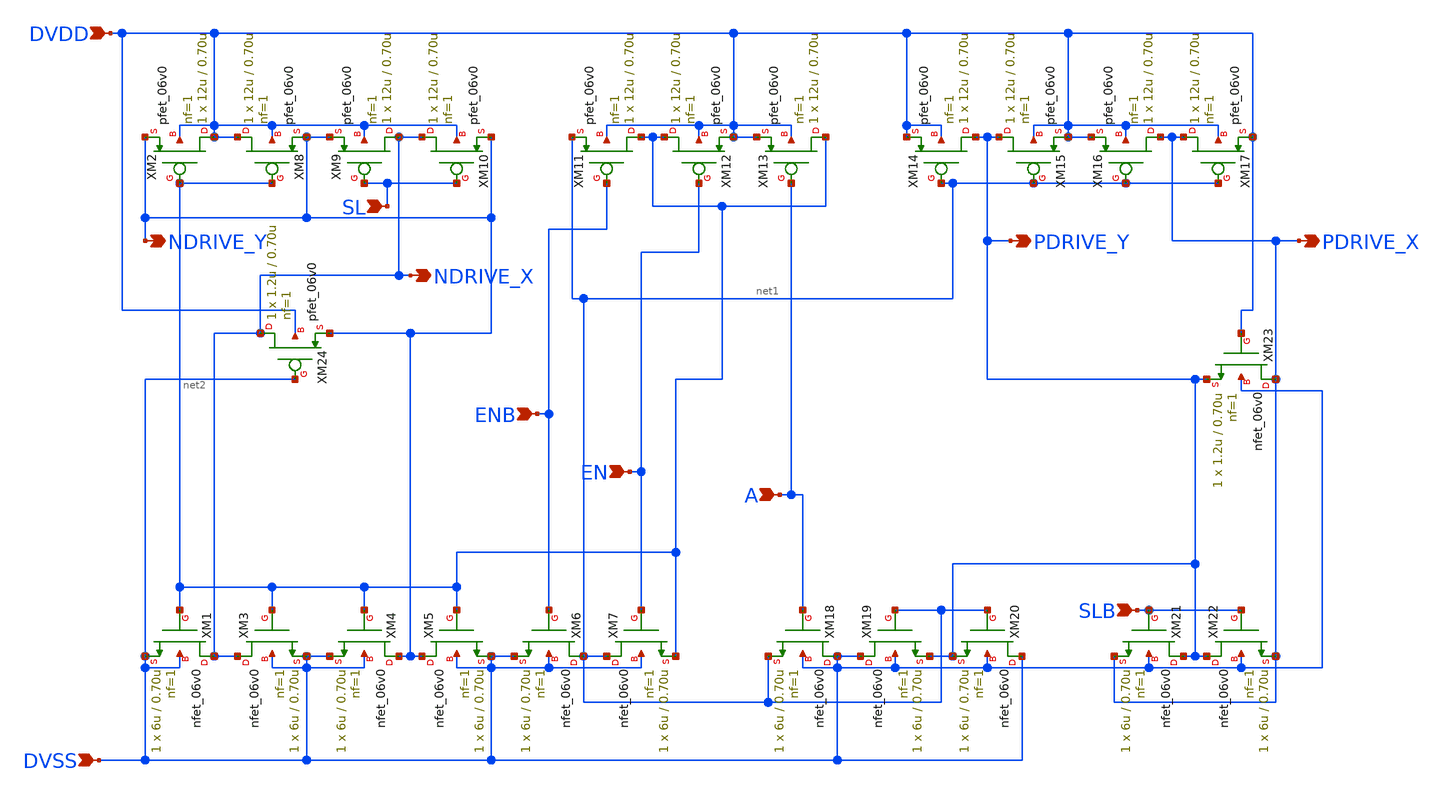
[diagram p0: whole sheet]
** sch_path: gf180mcu_fd_io__bi_24t/comp018green_out_predrv.sch
**.subckt comp018green_out_predrv DVSS DVDD SL ENB EN A SLB NDRIVE_X NDRIVE_Y PDRIVE_X PDRIVE_Y
*.ipin DVSS
*.ipin DVDD
*.ipin SL
*.ipin ENB
*.ipin EN
*.ipin A
*.ipin SLB
*.opin NDRIVE_X
*.opin NDRIVE_Y
*.opin PDRIVE_X
*.opin PDRIVE_Y
XM1 NDRIVE_X net2 DVSS DVSS nfet_06v0 L=0.70u W=6u nf=1 ad='int((nf+1)/2) * W/nf * 0.18u' as='int((nf+2)/2) * W/nf * 0.18u'
+ pd='2*int((nf+1)/2) * (W/nf + 0.18u)' ps='2*int((nf+2)/2) * (W/nf + 0.18u)' nrd='0.18u / W' nrs='0.18u / W'
+ sa=0 sb=0 sd=0 m=1
XM2 DVDD net2 NDRIVE_Y DVDD pfet_06v0 L=0.70u W=12u nf=1 ad='int((nf+1)/2) * W/nf * 0.18u' as='int((nf+2)/2) * W/nf * 0.18u'
+ pd='2*int((nf+1)/2) * (W/nf + 0.18u)' ps='2*int((nf+2)/2) * (W/nf + 0.18u)' nrd='0.18u / W' nrs='0.18u / W'
+ sa=0 sb=0 sd=0 m=1
XM3 NDRIVE_X net2 DVSS DVSS nfet_06v0 L=0.70u W=6u nf=1 ad='int((nf+1)/2) * W/nf * 0.18u' as='int((nf+2)/2) * W/nf * 0.18u'
+ pd='2*int((nf+1)/2) * (W/nf + 0.18u)' ps='2*int((nf+2)/2) * (W/nf + 0.18u)' nrd='0.18u / W' nrs='0.18u / W'
+ sa=0 sb=0 sd=0 m=1
XM4 NDRIVE_Y net2 DVSS DVSS nfet_06v0 L=0.70u W=6u nf=1 ad='int((nf+1)/2) * W/nf * 0.18u' as='int((nf+2)/2) * W/nf * 0.18u'
+ pd='2*int((nf+1)/2) * (W/nf + 0.18u)' ps='2*int((nf+2)/2) * (W/nf + 0.18u)' nrd='0.18u / W' nrs='0.18u / W'
+ sa=0 sb=0 sd=0 m=1
XM5 NDRIVE_Y net2 DVSS DVSS nfet_06v0 L=0.70u W=6u nf=1 ad='int((nf+1)/2) * W/nf * 0.18u' as='int((nf+2)/2) * W/nf * 0.18u'
+ pd='2*int((nf+1)/2) * (W/nf + 0.18u)' ps='2*int((nf+2)/2) * (W/nf + 0.18u)' nrd='0.18u / W' nrs='0.18u / W'
+ sa=0 sb=0 sd=0 m=1
XM6 net1 ENB DVSS DVSS nfet_06v0 L=0.70u W=6u nf=1 ad='int((nf+1)/2) * W/nf * 0.18u' as='int((nf+2)/2) * W/nf * 0.18u'
+ pd='2*int((nf+1)/2) * (W/nf + 0.18u)' ps='2*int((nf+2)/2) * (W/nf + 0.18u)' nrd='0.18u / W' nrs='0.18u / W'
+ sa=0 sb=0 sd=0 m=1
XM7 net1 EN net2 DVSS nfet_06v0 L=0.70u W=6u nf=1 ad='int((nf+1)/2) * W/nf * 0.18u' as='int((nf+2)/2) * W/nf * 0.18u'
+ pd='2*int((nf+1)/2) * (W/nf + 0.18u)' ps='2*int((nf+2)/2) * (W/nf + 0.18u)' nrd='0.18u / W' nrs='0.18u / W'
+ sa=0 sb=0 sd=0 m=1
XM8 DVDD net2 NDRIVE_Y DVDD pfet_06v0 L=0.70u W=12u nf=1 ad='int((nf+1)/2) * W/nf * 0.18u' as='int((nf+2)/2) * W/nf * 0.18u'
+ pd='2*int((nf+1)/2) * (W/nf + 0.18u)' ps='2*int((nf+2)/2) * (W/nf + 0.18u)' nrd='0.18u / W' nrs='0.18u / W'
+ sa=0 sb=0 sd=0 m=1
XM9 NDRIVE_X SL NDRIVE_Y DVDD pfet_06v0 L=0.70u W=12u nf=1 ad='int((nf+1)/2) * W/nf * 0.18u' as='int((nf+2)/2) * W/nf * 0.18u'
+ pd='2*int((nf+1)/2) * (W/nf + 0.18u)' ps='2*int((nf+2)/2) * (W/nf + 0.18u)' nrd='0.18u / W' nrs='0.18u / W'
+ sa=0 sb=0 sd=0 m=1
XM10 NDRIVE_X SL NDRIVE_Y DVDD pfet_06v0 L=0.70u W=12u nf=1 ad='int((nf+1)/2) * W/nf * 0.18u' as='int((nf+2)/2) * W/nf * 0.18u'
+ pd='2*int((nf+1)/2) * (W/nf + 0.18u)' ps='2*int((nf+2)/2) * (W/nf + 0.18u)' nrd='0.18u / W' nrs='0.18u / W'
+ sa=0 sb=0 sd=0 m=1
XM11 net2 ENB net1 DVDD pfet_06v0 L=0.70u W=12u nf=1 ad='int((nf+1)/2) * W/nf * 0.18u' as='int((nf+2)/2) * W/nf * 0.18u'
+ pd='2*int((nf+1)/2) * (W/nf + 0.18u)' ps='2*int((nf+2)/2) * (W/nf + 0.18u)' nrd='0.18u / W' nrs='0.18u / W'
+ sa=0 sb=0 sd=0 m=1
XM12 net2 EN DVDD DVDD pfet_06v0 L=0.70u W=12u nf=1 ad='int((nf+1)/2) * W/nf * 0.18u' as='int((nf+2)/2) * W/nf * 0.18u'
+ pd='2*int((nf+1)/2) * (W/nf + 0.18u)' ps='2*int((nf+2)/2) * (W/nf + 0.18u)' nrd='0.18u / W' nrs='0.18u / W'
+ sa=0 sb=0 sd=0 m=1
XM13 net2 A DVDD DVDD pfet_06v0 L=0.70u W=12u nf=1 ad='int((nf+1)/2) * W/nf * 0.18u' as='int((nf+2)/2) * W/nf * 0.18u'
+ pd='2*int((nf+1)/2) * (W/nf + 0.18u)' ps='2*int((nf+2)/2) * (W/nf + 0.18u)' nrd='0.18u / W' nrs='0.18u / W'
+ sa=0 sb=0 sd=0 m=1
XM14 PDRIVE_Y net1 DVDD DVDD pfet_06v0 L=0.70u W=12u nf=1 ad='int((nf+1)/2) * W/nf * 0.18u' as='int((nf+2)/2) * W/nf * 0.18u'
+ pd='2*int((nf+1)/2) * (W/nf + 0.18u)' ps='2*int((nf+2)/2) * (W/nf + 0.18u)' nrd='0.18u / W' nrs='0.18u / W'
+ sa=0 sb=0 sd=0 m=1
XM15 PDRIVE_Y net1 DVDD DVDD pfet_06v0 L=0.70u W=12u nf=1 ad='int((nf+1)/2) * W/nf * 0.18u' as='int((nf+2)/2) * W/nf * 0.18u'
+ pd='2*int((nf+1)/2) * (W/nf + 0.18u)' ps='2*int((nf+2)/2) * (W/nf + 0.18u)' nrd='0.18u / W' nrs='0.18u / W'
+ sa=0 sb=0 sd=0 m=1
XM16 PDRIVE_X net1 DVDD DVDD pfet_06v0 L=0.70u W=12u nf=1 ad='int((nf+1)/2) * W/nf * 0.18u' as='int((nf+2)/2) * W/nf * 0.18u'
+ pd='2*int((nf+1)/2) * (W/nf + 0.18u)' ps='2*int((nf+2)/2) * (W/nf + 0.18u)' nrd='0.18u / W' nrs='0.18u / W'
+ sa=0 sb=0 sd=0 m=1
XM17 PDRIVE_X net1 DVDD DVDD pfet_06v0 L=0.70u W=12u nf=1 ad='int((nf+1)/2) * W/nf * 0.18u' as='int((nf+2)/2) * W/nf * 0.18u'
+ pd='2*int((nf+1)/2) * (W/nf + 0.18u)' ps='2*int((nf+2)/2) * (W/nf + 0.18u)' nrd='0.18u / W' nrs='0.18u / W'
+ sa=0 sb=0 sd=0 m=1
XM18 DVSS A net1 DVSS nfet_06v0 L=0.70u W=6u nf=1 ad='int((nf+1)/2) * W/nf * 0.18u' as='int((nf+2)/2) * W/nf * 0.18u'
+ pd='2*int((nf+1)/2) * (W/nf + 0.18u)' ps='2*int((nf+2)/2) * (W/nf + 0.18u)' nrd='0.18u / W' nrs='0.18u / W'
+ sa=0 sb=0 sd=0 m=1
XM19 DVSS net1 PDRIVE_Y DVSS nfet_06v0 L=0.70u W=6u nf=1 ad='int((nf+1)/2) * W/nf * 0.18u' as='int((nf+2)/2) * W/nf * 0.18u'
+ pd='2*int((nf+1)/2) * (W/nf + 0.18u)' ps='2*int((nf+2)/2) * (W/nf + 0.18u)' nrd='0.18u / W' nrs='0.18u / W'
+ sa=0 sb=0 sd=0 m=1
XM20 DVSS net1 PDRIVE_Y DVSS nfet_06v0 L=0.70u W=6u nf=1 ad='int((nf+1)/2) * W/nf * 0.18u' as='int((nf+2)/2) * W/nf * 0.18u'
+ pd='2*int((nf+1)/2) * (W/nf + 0.18u)' ps='2*int((nf+2)/2) * (W/nf + 0.18u)' nrd='0.18u / W' nrs='0.18u / W'
+ sa=0 sb=0 sd=0 m=1
XM21 PDRIVE_Y SLB PDRIVE_X DVSS nfet_06v0 L=0.70u W=6u nf=1 ad='int((nf+1)/2) * W/nf * 0.18u' as='int((nf+2)/2) * W/nf * 0.18u'
+ pd='2*int((nf+1)/2) * (W/nf + 0.18u)' ps='2*int((nf+2)/2) * (W/nf + 0.18u)' nrd='0.18u / W' nrs='0.18u / W'
+ sa=0 sb=0 sd=0 m=1
XM22 PDRIVE_Y SLB PDRIVE_X DVSS nfet_06v0 L=0.70u W=6u nf=1 ad='int((nf+1)/2) * W/nf * 0.18u' as='int((nf+2)/2) * W/nf * 0.18u'
+ pd='2*int((nf+1)/2) * (W/nf + 0.18u)' ps='2*int((nf+2)/2) * (W/nf + 0.18u)' nrd='0.18u / W' nrs='0.18u / W'
+ sa=0 sb=0 sd=0 m=1
XM23 PDRIVE_X DVDD PDRIVE_Y DVSS nfet_06v0 L=0.70u W=1.2u nf=1 ad='int((nf+1)/2) * W/nf * 0.18u' as='int((nf+2)/2) * W/nf * 0.18u'
+ pd='2*int((nf+1)/2) * (W/nf + 0.18u)' ps='2*int((nf+2)/2) * (W/nf + 0.18u)' nrd='0.18u / W' nrs='0.18u / W'
+ sa=0 sb=0 sd=0 m=1
XM24 NDRIVE_X DVSS NDRIVE_Y DVDD pfet_06v0 L=0.70u W=1.2u nf=1 ad='int((nf+1)/2) * W/nf * 0.18u' as='int((nf+2)/2) * W/nf * 0.18u'
+ pd='2*int((nf+1)/2) * (W/nf + 0.18u)' ps='2*int((nf+2)/2) * (W/nf + 0.18u)' nrd='0.18u / W' nrs='0.18u / W'
+ sa=0 sb=0 sd=0 m=1
**.ends
.end
